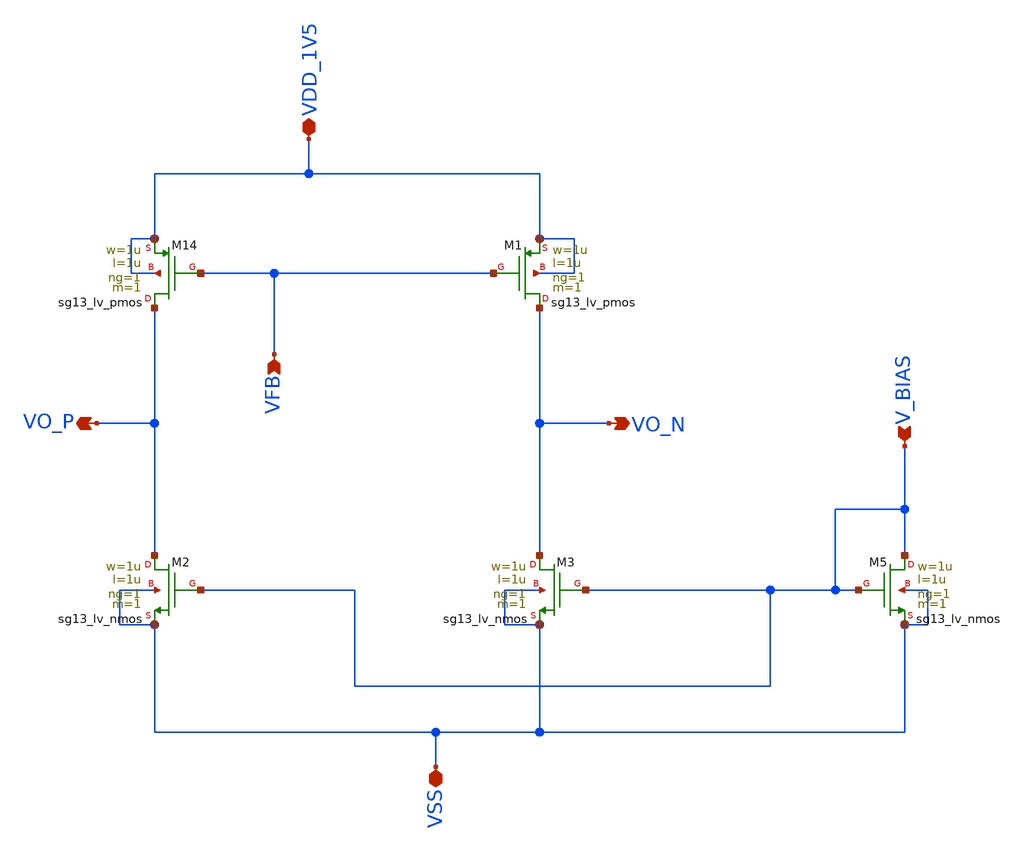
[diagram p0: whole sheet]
** sch_path: cmfb.sch
**.subckt cmfb VDD_1V5 VSS V_BIAS VFB VO_P VO_N
*.iopin VDD_1V5
*.iopin VSS
*.ipin V_BIAS
*.ipin VFB
*.opin VO_P
*.opin VO_N
XM14 VO_P VFB VDD_1V5 VDD_1V5 sg13_lv_pmos w=1u l=1u ng=1 m=1 mm_ok=1
XM1 VO_N VFB VDD_1V5 VDD_1V5 sg13_lv_pmos w=1u l=1u ng=1 m=1 mm_ok=1
XM2 VO_P V_BIAS VSS VSS sg13_lv_nmos w=1u l=1u ng=1 m=1 mm_ok=1
XM3 VO_N V_BIAS VSS VSS sg13_lv_nmos w=1u l=1u ng=1 m=1 mm_ok=1
XM5 V_BIAS V_BIAS VSS VSS sg13_lv_nmos w=1u l=1u ng=1 m=1 mm_ok=1
**.ends
.end
